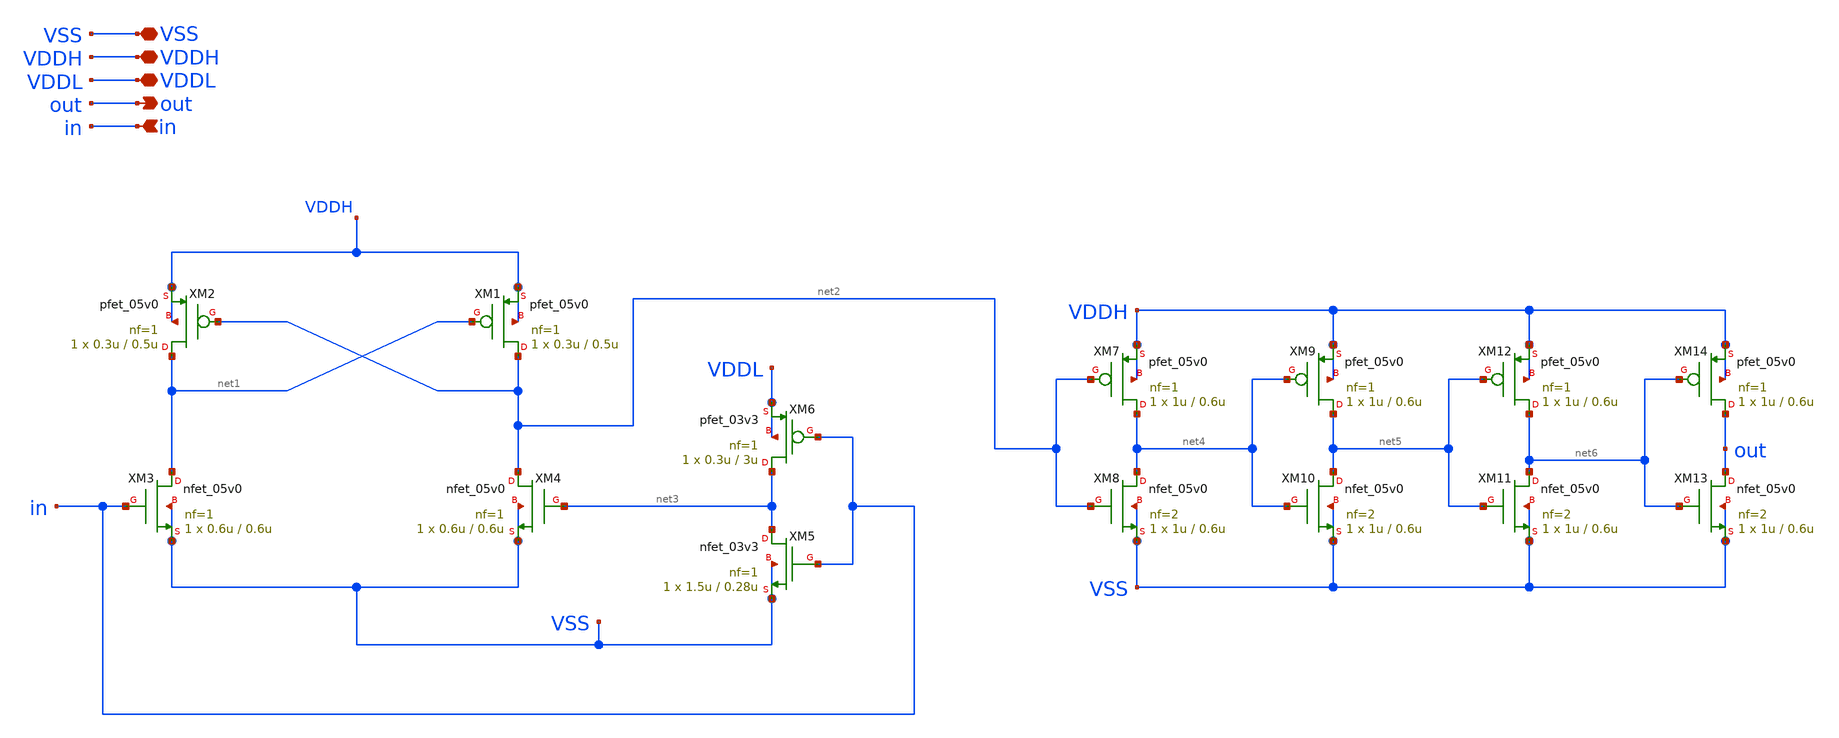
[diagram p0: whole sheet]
** sch_path: designs/libs/core_vco/vco_ls1v8_5/vco_ls1v8_5.sch
**.subckt vco_ls1v8_5 VDDH VDDL out VSS in
*.iopin VDDH
*.iopin VDDL
*.opin out
*.iopin VSS
*.ipin in
XM1 net2 net1 VDDH VDDH pfet_05v0 L=0.5u W=0.3u nf=1 ad='int((nf+1)/2) * W/nf * 0.18u' as='int((nf+2)/2) * W/nf * 0.18u'
+ pd='2*int((nf+1)/2) * (W/nf + 0.18u)' ps='2*int((nf+2)/2) * (W/nf + 0.18u)' nrd='0.18u / W' nrs='0.18u / W'
+ sa=0 sb=0 sd=0 m=1
XM2 net1 net2 VDDH VDDH pfet_05v0 L=0.5u W=0.3u nf=1 ad='int((nf+1)/2) * W/nf * 0.18u' as='int((nf+2)/2) * W/nf * 0.18u'
+ pd='2*int((nf+1)/2) * (W/nf + 0.18u)' ps='2*int((nf+2)/2) * (W/nf + 0.18u)' nrd='0.18u / W' nrs='0.18u / W'
+ sa=0 sb=0 sd=0 m=1
XM3 net1 in VSS VSS nfet_05v0 L=0.6u W=0.6u nf=1 ad='int((nf+1)/2) * W/nf * 0.18u' as='int((nf+2)/2) * W/nf * 0.18u'
+ pd='2*int((nf+1)/2) * (W/nf + 0.18u)' ps='2*int((nf+2)/2) * (W/nf + 0.18u)' nrd='0.18u / W' nrs='0.18u / W'
+ sa=0 sb=0 sd=0 m=1
XM4 net2 net3 VSS VSS nfet_05v0 L=0.6u W=0.6u nf=1 ad='int((nf+1)/2) * W/nf * 0.18u' as='int((nf+2)/2) * W/nf * 0.18u'
+ pd='2*int((nf+1)/2) * (W/nf + 0.18u)' ps='2*int((nf+2)/2) * (W/nf + 0.18u)' nrd='0.18u / W' nrs='0.18u / W'
+ sa=0 sb=0 sd=0 m=1
XM5 net3 in VSS VSS nfet_03v3 L=0.28u W=1.5u nf=1 ad='int((nf+1)/2) * W/nf * 0.18u' as='int((nf+2)/2) * W/nf * 0.18u'
+ pd='2*int((nf+1)/2) * (W/nf + 0.18u)' ps='2*int((nf+2)/2) * (W/nf + 0.18u)' nrd='0.18u / W' nrs='0.18u / W'
+ sa=0 sb=0 sd=0 m=1
XM6 net3 in VDDL VDDL pfet_03v3 L=3u W=0.3u nf=1 ad='int((nf+1)/2) * W/nf * 0.18u' as='int((nf+2)/2) * W/nf * 0.18u'
+ pd='2*int((nf+1)/2) * (W/nf + 0.18u)' ps='2*int((nf+2)/2) * (W/nf + 0.18u)' nrd='0.18u / W' nrs='0.18u / W'
+ sa=0 sb=0 sd=0 m=1
XM7 net4 net2 VDDH VDDH pfet_05v0 L=0.6u W=1u nf=1 ad='int((nf+1)/2) * W/nf * 0.18u' as='int((nf+2)/2) * W/nf * 0.18u'
+ pd='2*int((nf+1)/2) * (W/nf + 0.18u)' ps='2*int((nf+2)/2) * (W/nf + 0.18u)' nrd='0.18u / W' nrs='0.18u / W'
+ sa=0 sb=0 sd=0 m=1
XM8 net4 net2 VSS VSS nfet_05v0 L=0.6u W=1u nf=2 ad='int((nf+1)/2) * W/nf * 0.18u' as='int((nf+2)/2) * W/nf * 0.18u'
+ pd='2*int((nf+1)/2) * (W/nf + 0.18u)' ps='2*int((nf+2)/2) * (W/nf + 0.18u)' nrd='0.18u / W' nrs='0.18u / W'
+ sa=0 sb=0 sd=0 m=1
XM9 net5 net4 VDDH VDDH pfet_05v0 L=0.6u W=1u nf=1 ad='int((nf+1)/2) * W/nf * 0.18u' as='int((nf+2)/2) * W/nf * 0.18u'
+ pd='2*int((nf+1)/2) * (W/nf + 0.18u)' ps='2*int((nf+2)/2) * (W/nf + 0.18u)' nrd='0.18u / W' nrs='0.18u / W'
+ sa=0 sb=0 sd=0 m=1
XM12 net6 net5 VDDH VDDH pfet_05v0 L=0.6u W=1u nf=1 ad='int((nf+1)/2) * W/nf * 0.18u' as='int((nf+2)/2) * W/nf * 0.18u'
+ pd='2*int((nf+1)/2) * (W/nf + 0.18u)' ps='2*int((nf+2)/2) * (W/nf + 0.18u)' nrd='0.18u / W' nrs='0.18u / W'
+ sa=0 sb=0 sd=0 m=1
XM14 out net6 VDDH VDDH pfet_05v0 L=0.6u W=1u nf=1 ad='int((nf+1)/2) * W/nf * 0.18u' as='int((nf+2)/2) * W/nf * 0.18u'
+ pd='2*int((nf+1)/2) * (W/nf + 0.18u)' ps='2*int((nf+2)/2) * (W/nf + 0.18u)' nrd='0.18u / W' nrs='0.18u / W'
+ sa=0 sb=0 sd=0 m=1
XM10 net5 net4 VSS VSS nfet_05v0 L=0.6u W=1u nf=2 ad='int((nf+1)/2) * W/nf * 0.18u' as='int((nf+2)/2) * W/nf * 0.18u'
+ pd='2*int((nf+1)/2) * (W/nf + 0.18u)' ps='2*int((nf+2)/2) * (W/nf + 0.18u)' nrd='0.18u / W' nrs='0.18u / W'
+ sa=0 sb=0 sd=0 m=1
XM11 net6 net5 VSS VSS nfet_05v0 L=0.6u W=1u nf=2 ad='int((nf+1)/2) * W/nf * 0.18u' as='int((nf+2)/2) * W/nf * 0.18u'
+ pd='2*int((nf+1)/2) * (W/nf + 0.18u)' ps='2*int((nf+2)/2) * (W/nf + 0.18u)' nrd='0.18u / W' nrs='0.18u / W'
+ sa=0 sb=0 sd=0 m=1
XM13 out net6 VSS VSS nfet_05v0 L=0.6u W=1u nf=2 ad='int((nf+1)/2) * W/nf * 0.18u' as='int((nf+2)/2) * W/nf * 0.18u'
+ pd='2*int((nf+1)/2) * (W/nf + 0.18u)' ps='2*int((nf+2)/2) * (W/nf + 0.18u)' nrd='0.18u / W' nrs='0.18u / W'
+ sa=0 sb=0 sd=0 m=1
**.ends
.end
